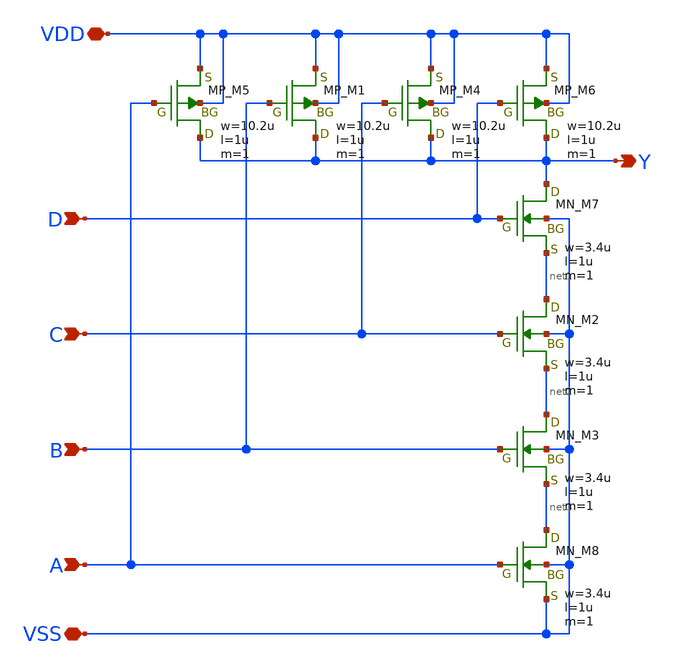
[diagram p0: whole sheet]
** sch_path: member_project/imager/YuMaehashi/design/pulsegen_nand4.sch
**.subckt pulsegen_nand4 B A Y VSS VDD C D
*.ipin B
*.ipin A
*.opin Y
*.iopin VSS
*.iopin VDD
*.ipin C
*.ipin D
XM1 Y B VDD VDD PMOS w=10.2u l=1u as=0 ad=0 ps=0 pd=0 nrd=0 nrs=0 m=1
XM4 Y C VDD VDD PMOS w=10.2u l=1u as=0 ad=0 ps=0 pd=0 nrd=0 nrs=0 m=1
XM6 Y D VDD VDD PMOS w=10.2u l=1u as=0 ad=0 ps=0 pd=0 nrd=0 nrs=0 m=1
XM7 Y D net1 VSS NMOS w=3.4u l=1u as=0 ad=0 ps=0 pd=0 nrd=0 nrs=0 m=1
XM2 net1 C net2 VSS NMOS w=3.4u l=1u as=0 ad=0 ps=0 pd=0 nrd=0 nrs=0 m=1
XM3 net2 B net3 VSS NMOS w=3.4u l=1u as=0 ad=0 ps=0 pd=0 nrd=0 nrs=0 m=1
XM5 Y A VDD VDD PMOS w=10.2u l=1u as=0 ad=0 ps=0 pd=0 nrd=0 nrs=0 m=1
XM8 net3 A VSS VSS NMOS w=3.4u l=1u as=0 ad=0 ps=0 pd=0 nrd=0 nrs=0 m=1
**.ends
.end
